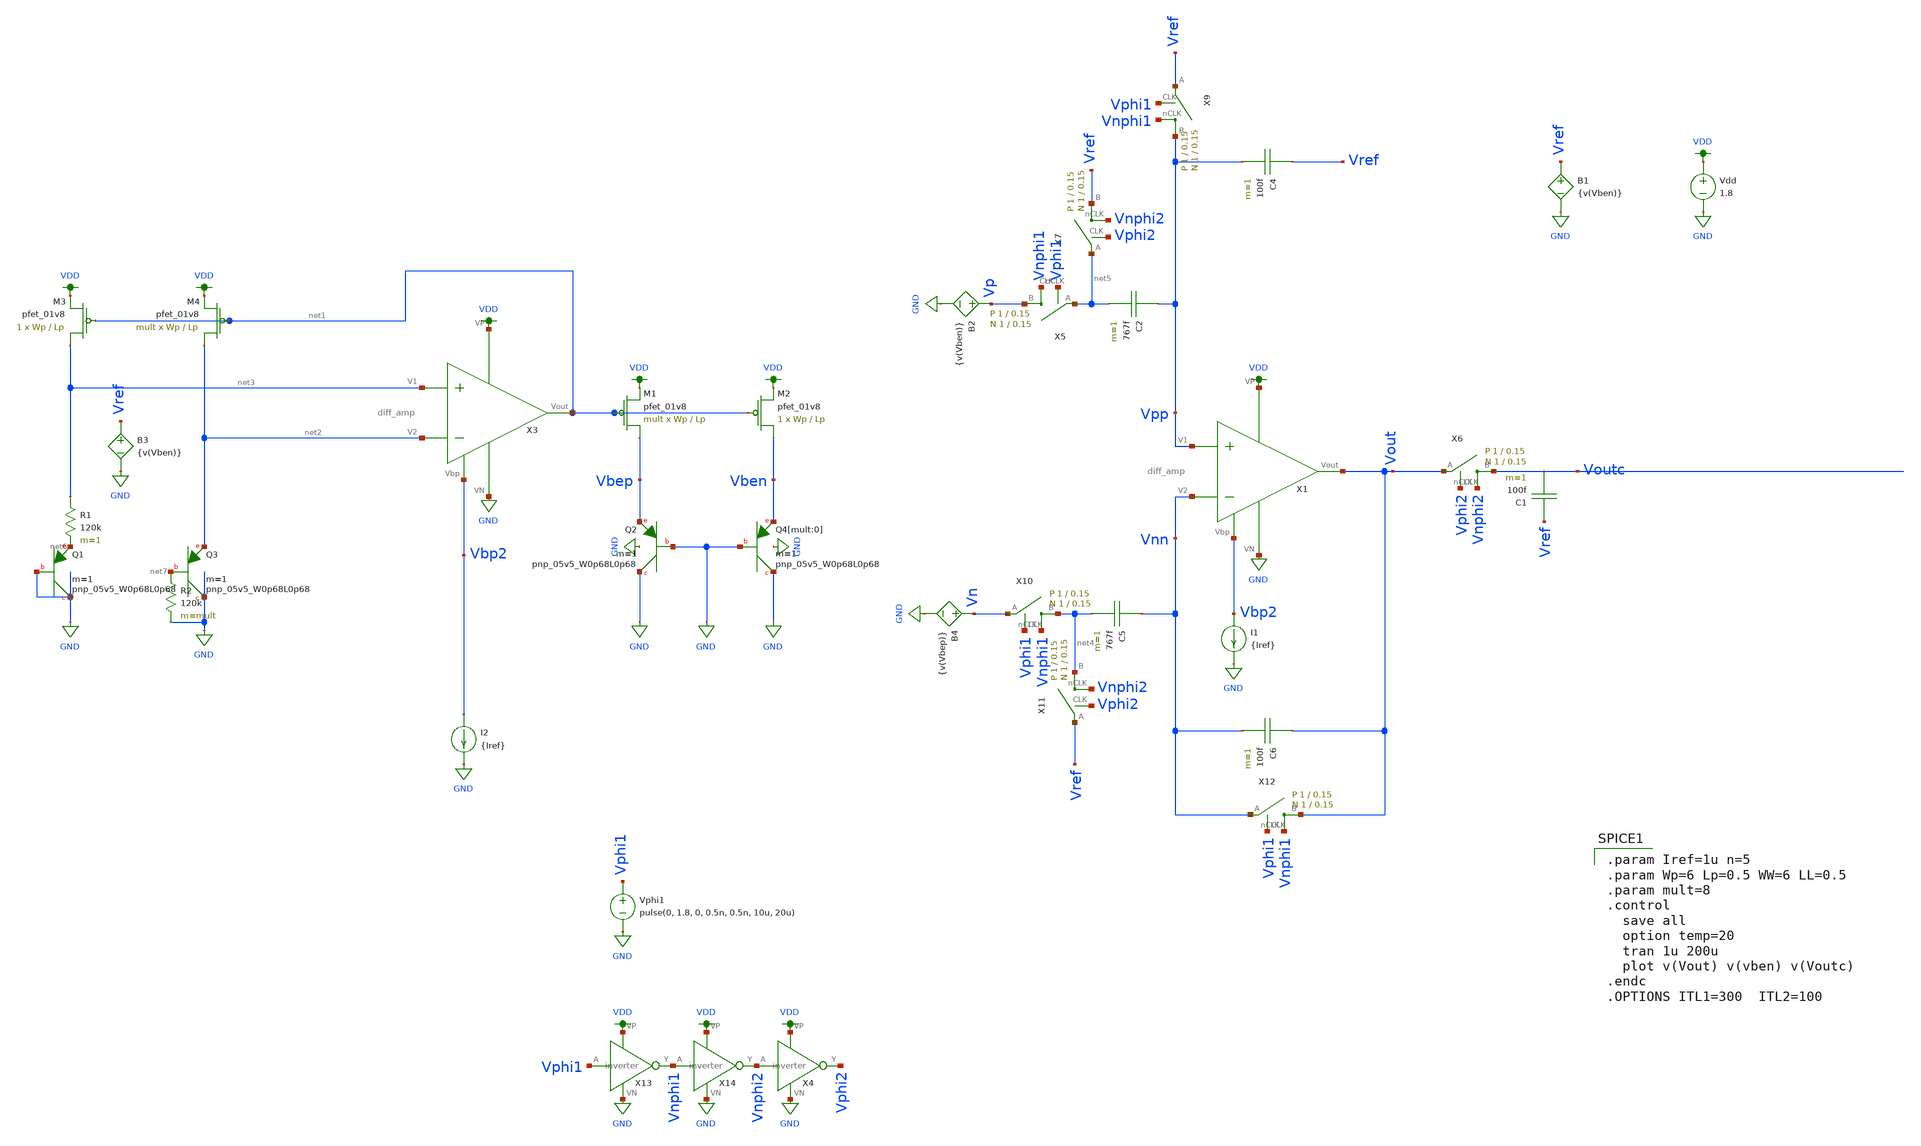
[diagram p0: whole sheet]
** sch_path: schematic/test/archive/bandgap_dctempaltamp.sch
**.subckt bandgap_dctempaltamp
XQ2 GND GND Vbep sky130_fd_pr__pnp_05v5_W0p68L0p68 m=1
XM1 Vbep net1 VDD VDD sky130_fd_pr__pfet_01v8 L=Lp W=Wp nf=1 ad='int((nf+1)/2) * W/nf * 0.29' as='int((nf+2)/2) * W/nf * 0.29'
+ pd='2*int((nf+1)/2) * (W/nf + 0.29)' ps='2*int((nf+2)/2) * (W/nf + 0.29)' nrd='0.29 / W' nrs='0.29 / W'
+ sa=0 sb=0 sd=0 mult=mult m=mult
XM2 Vben net1 VDD VDD sky130_fd_pr__pfet_01v8 L=Lp W=Wp nf=1 ad='int((nf+1)/2) * W/nf * 0.29' as='int((nf+2)/2) * W/nf * 0.29'
+ pd='2*int((nf+1)/2) * (W/nf + 0.29)' ps='2*int((nf+2)/2) * (W/nf + 0.29)' nrd='0.29 / W' nrs='0.29 / W'
+ sa=0 sb=0 sd=0 mult=1 m=1
XQ4[mult:0] GND GND Vben sky130_fd_pr__pnp_05v5_W0p68L0p68 m=1
XQ1 GND GND net6 sky130_fd_pr__pnp_05v5_W0p68L0p68 m=1
XQ3 GND net7 net2 sky130_fd_pr__pnp_05v5_W0p68L0p68 m=1
R1 net3 net6 120k m=1
R2 net7 GND 120k m=mult
XM3 net3 net1 VDD VDD sky130_fd_pr__pfet_01v8 L=Lp W=Wp nf=1 ad='int((nf+1)/2) * W/nf * 0.29' as='int((nf+2)/2) * W/nf * 0.29'
+ pd='2*int((nf+1)/2) * (W/nf + 0.29)' ps='2*int((nf+2)/2) * (W/nf + 0.29)' nrd='0.29 / W' nrs='0.29 / W'
+ sa=0 sb=0 sd=0 mult=1 m=1
XM4 net2 net1 VDD VDD sky130_fd_pr__pfet_01v8 L=Lp W=Wp nf=1 ad='int((nf+1)/2) * W/nf * 0.29' as='int((nf+2)/2) * W/nf * 0.29'
+ pd='2*int((nf+1)/2) * (W/nf + 0.29)' ps='2*int((nf+2)/2) * (W/nf + 0.29)' nrd='0.29 / W' nrs='0.29 / W'
+ sa=0 sb=0 sd=0 mult=mult m=mult
X3 VDD Vbp2 net1 net3 net2 GND diff_amp
I2 Vbp2 GND {Iref}
Vphi1 Vphi1 GND pulse(0, 1.8, 0, 0.5n, 0.5n, 10u, 20u)
X13 Vphi1 Vnphi1 VDD GND inverter
X14 Vnphi1 Vnphi2 VDD GND inverter
X4 Vnphi2 Vphi2 VDD GND inverter
B3 Vref GND V={v(Vben)}
Vdd VDD GND 1.8
C5 Vnn net4 767f m=1
C6 Vout Vnn 100f m=1
X10 net4 Vn Vphi1 Vnphi1 switch Wp=1 Lp=0.15 WW=1 LL=0.15
X11 net4 Vref Vphi2 Vnphi2 switch Wp=1 Lp=0.15 WW=1 LL=0.15
X12 Vout Vnn Vphi1 Vnphi1 switch Wp=1 Lp=0.15 WW=1 LL=0.15
C2 Vpp net5 767f m=1
C4 Vref Vpp 100f m=1
X5 Vp net5 Vphi1 Vnphi1 switch Wp=1 Lp=0.15 WW=1 LL=0.15
X7 Vref net5 Vphi2 Vnphi2 switch Wp=1 Lp=0.15 WW=1 LL=0.15
X9 Vpp Vref Vphi1 Vnphi1 switch Wp=1 Lp=0.15 WW=1 LL=0.15
B1 Vref GND V={v(Vben)}
B2 Vp GND V={v(Vben)}
X1 VDD Vbp2 Vout Vpp Vnn GND diff_amp
I1 Vbp2 GND {Iref}
C1 Vref Voutc 100f m=1
X6 Voutc Vout Vphi2 Vnphi2 switch Wp=1 Lp=0.15 WW=1 LL=0.15
B4 Vn GND V={v(Vbep)}
**** begin user architecture code

.param Iref=1u n=5
.param Wp=6 Lp=0.5 WW=6 LL=0.5
.param mult=8
.control
  save all
  let startTemp = 10
  let currTemp = startTemp
  let endTemp = 100
  let dt = 1
  set appendwrite = FALSE
  set wr_vecnames
  while currTemp <= endTemp
    destroy
    set appendwrite = FALSE
    option temp=$&currTemp
    tran 1u 200u
    wrdata /home/madvlsi/Documents/MADVLSI-Final_Project/schematic/data/SCbandgap{$&currTemp}C7p67refVben.csv
+ v(vbep) v(vben) v(vout) v(vphi1) v(vphi2) v(vref) currTemp
    let currTemp = currTemp + dt
  end
.endc
.OPTIONS ITL1=300  ITL2=100


.option wnflag=1
.param MC_SWITCH=0.0
.lib /media/qdeng/526448C32060CF5C/skywater/skywater-pdk/libraries/sky130_fd_pr_ngspice/latest/models/sky130.lib.spice tt


.param Iref=1u n=5
.param Wp=6 Lp=0.5 WW=6 LL=0.5
.param mult=8
.control
  save all
  option temp=20
  tran 1u 200u
  plot v(Vout) v(vben) v(Voutc)
.endc
.OPTIONS ITL1=300  ITL2=100

**** end user architecture code
**.ends
.GLOBAL VDD
.GLOBAL GND
.end
